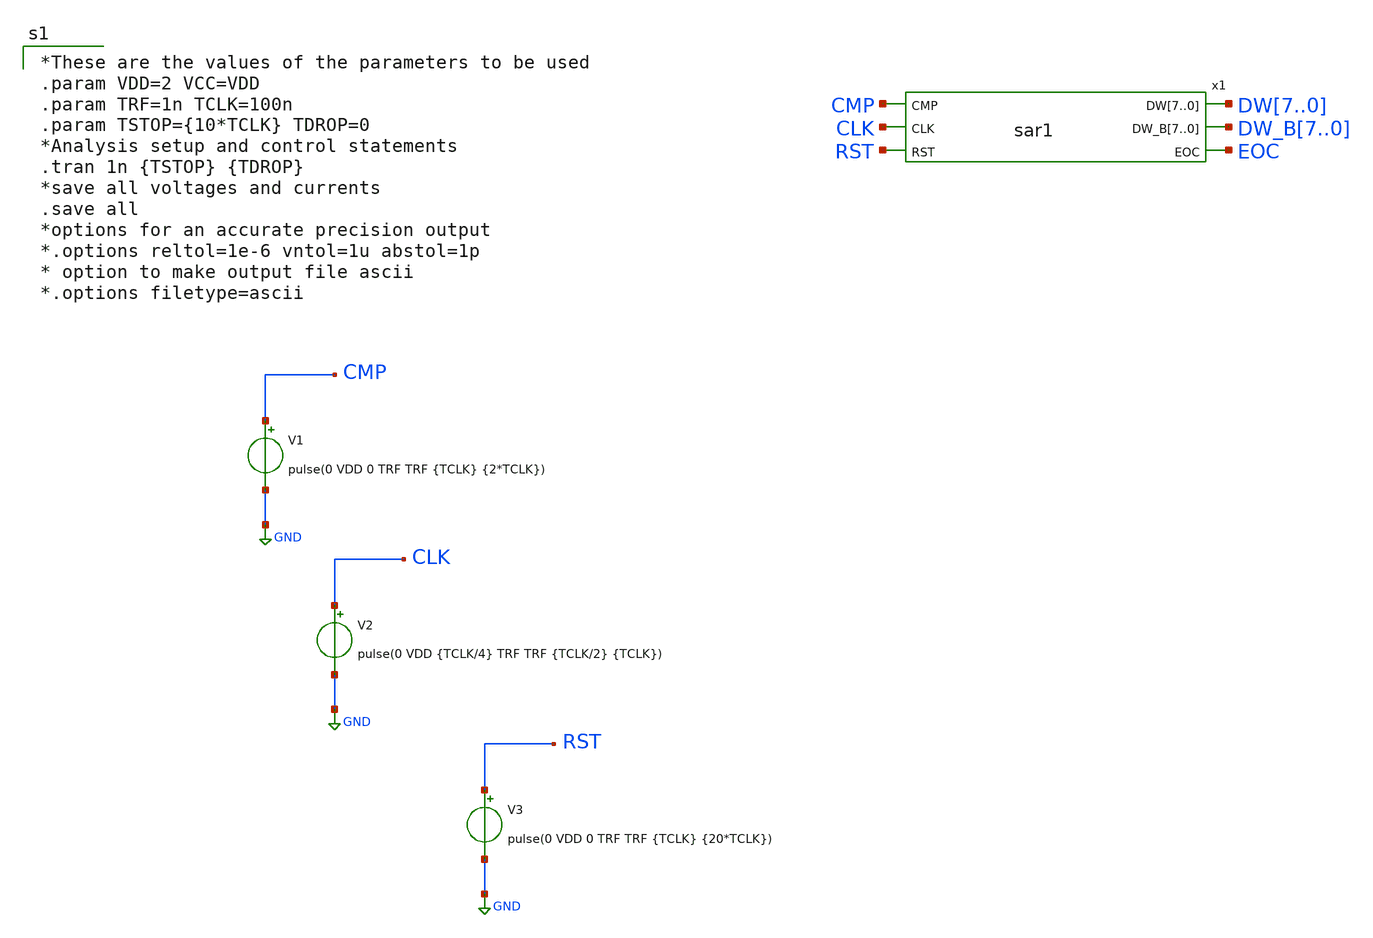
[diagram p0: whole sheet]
** sch_path: sar1_tb.sch
**.subckt sar1_tb
x1 CMP CLK RST DW7 DW6 DW5 DW4 DW3 DW2 DW1 DW0 DW_B7 DW_B6 DW_B5 DW_B4 DW_B3 DW_B2 DW_B1 DW_B0 EOC
+ sar1
V1 CMP GND pulse(0 VDD 0 TRF TRF {TCLK} {2*TCLK})
V2 CLK GND pulse(0 VDD {TCLK/4} TRF TRF {TCLK/2} {TCLK})
V3 RST GND pulse(0 VDD 0 TRF TRF {TCLK} {20*TCLK})
**** begin user architecture code

*These are the values of the parameters to be used
.param VDD=2 VCC=VDD
.param TRF=1n TCLK=100n
.param TSTOP={10*TCLK} TDROP=0
*Analysis setup and control statements
.tran 1n {TSTOP} {TDROP}
*save all voltages and currents
.save all
*options for an accurate precision output
*.options reltol=1e-6 vntol=1u abstol=1p
* option to make output file ascii
*.options filetype=ascii


**** end user architecture code
**.ends

* expanding   symbol:  sar1.sym # of pins=6
** sym_path: sar1.sym
** sch_path: sar1.sch
.subckt sar1 CMP CLK RST DW7 DW6 DW5 DW4 DW3 DW2 DW1 DW0 DW_B7 DW_B6 DW_B5 DW_B4 DW_B3 DW_B2 DW_B1
+ DW_B0 EOC
*.ipin CMP
*.ipin CLK
*.ipin RST
*.opin DW7,DW6,DW5,DW4,DW3,DW2,DW1,DW0
*.opin DW_B7,DW_B6,DW_B5,DW_B4,DW_B3,DW_B2,DW_B1,DW_B0
*.opin EOC
xRING_CNT8 VLOW CLK QCNT8 RST Q_B8 VLOW dff
xRING_CNT7 QCNT8 CLK QCNT7 VLOW Q_B7 RST dff
xRING_CNT6 QCNT7 CLK QCNT6 VLOW Q_B6 RST dff
xRING_CNT5 QCNT6 CLK QCNT5 VLOW Q_B5 RST dff
xRING_CNT4 QCNT5 CLK QCNT4 VLOW Q_B4 RST dff
xRING_CNT3 QCNT4 CLK QCNT3 VLOW Q_B3 RST dff
xRING_CNT2 QCNT3 CLK QCNT2 VLOW Q_B2 RST dff
xRING_CNT1 QCNT2 CLK QCNT1 VLOW Q_B1 RST dff
xRING_CNT0 QCNT1 CLK QCNT0 VLOW Q_B0 RST dff
xCODE_REG7 CMP DW6 DW7 QCNT8 DW_B7 VLOW dff
xCODE_REG6 CMP DW5 DW6 QCNT7 DW_B6 RST dff
xCODE_REG5 CMP DW4 DW5 QCNT6 DW_B5 RST dff
xCODE_REG4 CMP DW3 DW4 QCNT5 DW_B4 RST dff
xCODE_REG3 CMP DW2 DW3 QCNT4 DW_B3 RST dff
xCODE_REG2 CMP DW1 DW2 QCNT3 DW_B2 RST dff
xCODE_REG1 CMP DW0 DW1 QCNT2 DW_B1 RST dff
xCODE_REG0 CMP EOC DW0 QCNT1 DW_B0 RST dff
x3 VLOW VLOW EOC QCNT0 net1 RST dff
**** begin user architecture code

V1 VLOW 0 0


**** end user architecture code
.ends


* expanding   symbol:  dff.sym # of pins=6
** sym_path: dff.sym
** sch_path: dff.sch
.subckt dff D CLK Q SET QB RST
*.ipin D
*.ipin CLK
*.ipin SET
*.ipin RST
*.opin Q
*.opin QB
**** begin user architecture code

a1 D CLK SET RST Qi QBi flop1
.model flop1 d_dff(clk_delay = 1e-9 set_delay = 1e-9  reset_delay = 1e-9 ic = 2 rise_delay = 1e-9
+  fall_delay = 1e-9)

v1 Qi Q 0
V2 QBi QB 0


**** end user architecture code
.ends

.GLOBAL GND
.end
